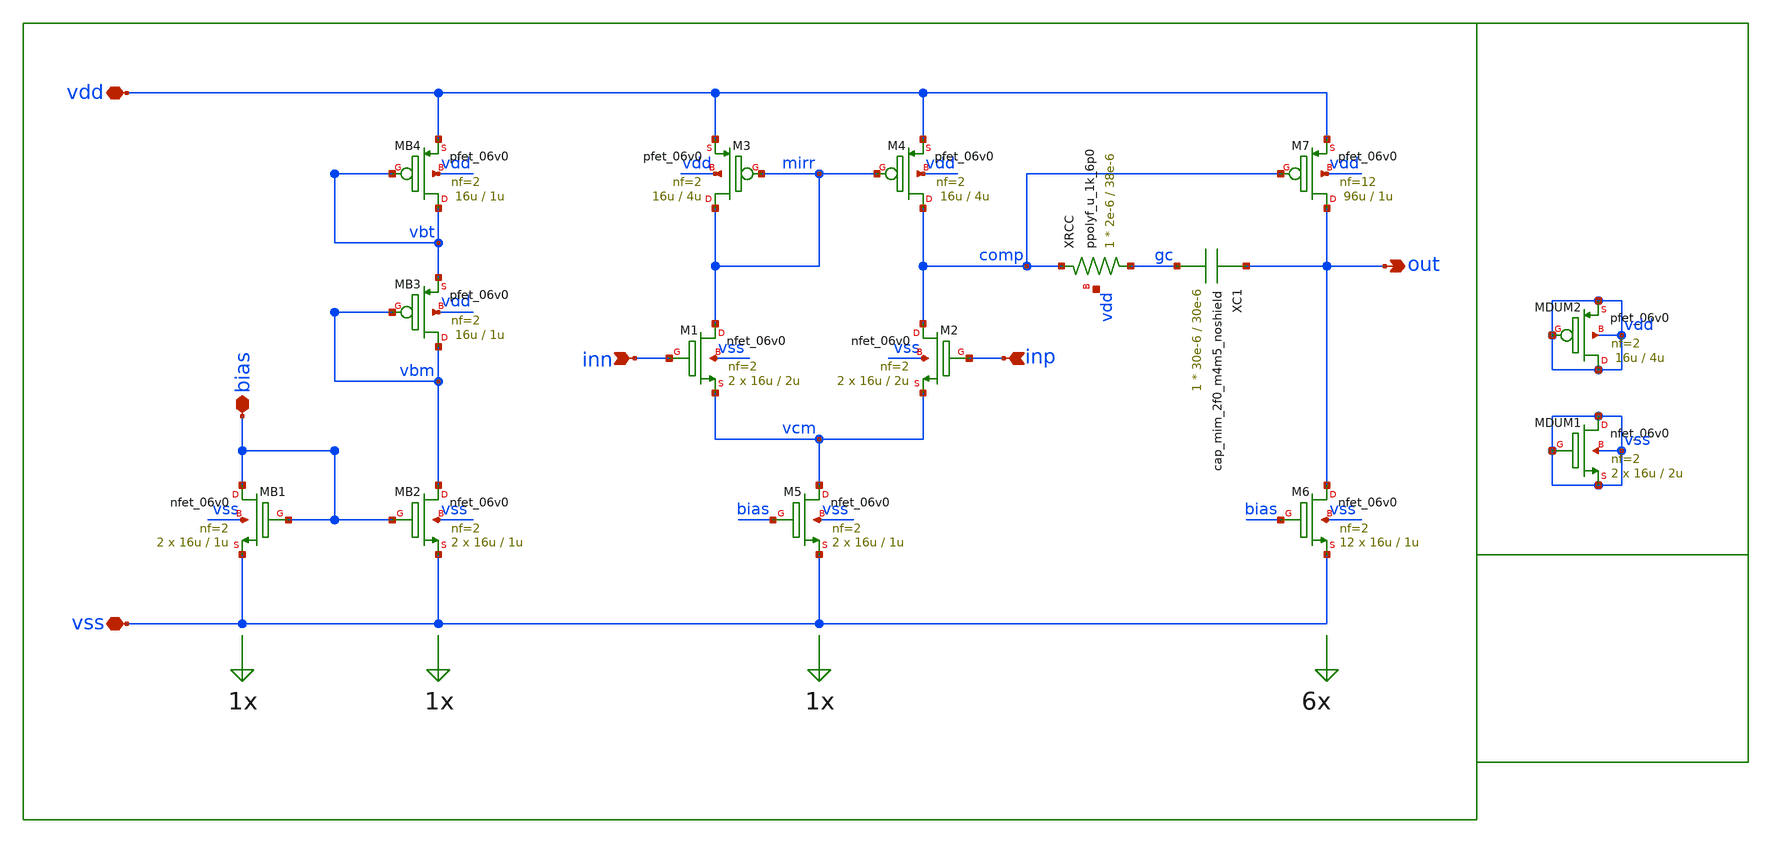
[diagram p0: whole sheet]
** sch_path: xschem/sch/testbuffer/tb_amplifier/tb_amplifier.sch
**.subckt tb_amplifier inn inp out bias vdd vss
*.ipin inn
*.ipin inp
*.opin out
*.iopin bias
*.iopin vdd
*.iopin vss
XM3 mirr mirr vdd vdd pfet_06v0 L=4u W=16u nf=2 ad='int((nf+1)/2) * W/nf * 0.18u' as='int((nf+2)/2) * W/nf * 0.18u'
+ pd='2*int((nf+1)/2) * (W/nf + 0.18u)' ps='2*int((nf+2)/2) * (W/nf + 0.18u)' nrd='0.18u / W' nrs='0.18u / W'
+ sa=0 sb=0 sd=0 m=2 par=2
XM4 comp mirr vdd vdd pfet_06v0 L=4u W=16u nf=2 ad='int((nf+1)/2) * W/nf * 0.18u' as='int((nf+2)/2) * W/nf * 0.18u'
+ pd='2*int((nf+1)/2) * (W/nf + 0.18u)' ps='2*int((nf+2)/2) * (W/nf + 0.18u)' nrd='0.18u / W' nrs='0.18u / W'
+ sa=0 sb=0 sd=0 m=2 par=2
XM2 comp inp vcm vss nfet_06v0 L=2u W=16u nf=2 ad='int((nf+1)/2) * W/nf * 0.18u' as='int((nf+2)/2) * W/nf * 0.18u'
+ pd='2*int((nf+1)/2) * (W/nf + 0.18u)' ps='2*int((nf+2)/2) * (W/nf + 0.18u)' nrd='0.18u / W' nrs='0.18u / W'
+ sa=0 sb=0 sd=0 m=2 par=2
XM1 mirr inn vcm vss nfet_06v0 L=2u W=16u nf=2 ad='int((nf+1)/2) * W/nf * 0.18u' as='int((nf+2)/2) * W/nf * 0.18u'
+ pd='2*int((nf+1)/2) * (W/nf + 0.18u)' ps='2*int((nf+2)/2) * (W/nf + 0.18u)' nrd='0.18u / W' nrs='0.18u / W'
+ sa=0 sb=0 sd=0 m=2 par=2
XM5 vcm bias vss vss nfet_06v0 L=1u W=16u nf=2 ad='int((nf+1)/2) * W/nf * 0.18u' as='int((nf+2)/2) * W/nf * 0.18u'
+ pd='2*int((nf+1)/2) * (W/nf + 0.18u)' ps='2*int((nf+2)/2) * (W/nf + 0.18u)' nrd='0.18u / W' nrs='0.18u / W'
+ sa=0 sb=0 sd=0 m=2 par=2
XM6 out bias vss vss nfet_06v0 L=1u W=16u nf=2 ad='int((nf+1)/2) * W/nf * 0.18u' as='int((nf+2)/2) * W/nf * 0.18u'
+ pd='2*int((nf+1)/2) * (W/nf + 0.18u)' ps='2*int((nf+2)/2) * (W/nf + 0.18u)' nrd='0.18u / W' nrs='0.18u / W'
+ sa=0 sb=0 sd=0 m=12 par=12
XM7 out comp vdd vdd pfet_06v0 L=1u W=96u nf=12 ad='int((nf+1)/2) * W/nf * 0.18u' as='int((nf+2)/2) * W/nf * 0.18u'
+ pd='2*int((nf+1)/2) * (W/nf + 0.18u)' ps='2*int((nf+2)/2) * (W/nf + 0.18u)' nrd='0.18u / W' nrs='0.18u / W'
+ sa=0 sb=0 sd=0 m=1 par=1
XMB1 bias bias vss vss nfet_06v0 L=1u W=16u nf=2 ad='int((nf+1)/2) * W/nf * 0.18u' as='int((nf+2)/2) * W/nf * 0.18u'
+ pd='2*int((nf+1)/2) * (W/nf + 0.18u)' ps='2*int((nf+2)/2) * (W/nf + 0.18u)' nrd='0.18u / W' nrs='0.18u / W'
+ sa=0 sb=0 sd=0 m=2 par=2
XMB2 vbm bias vss vss nfet_06v0 L=1u W=16u nf=2 ad='int((nf+1)/2) * W/nf * 0.18u' as='int((nf+2)/2) * W/nf * 0.18u'
+ pd='2*int((nf+1)/2) * (W/nf + 0.18u)' ps='2*int((nf+2)/2) * (W/nf + 0.18u)' nrd='0.18u / W' nrs='0.18u / W'
+ sa=0 sb=0 sd=0 m=2 par=2
XMB3 vbm vbm vbt vdd pfet_06v0 L=1u W=16u nf=2 ad='int((nf+1)/2) * W/nf * 0.18u' as='int((nf+2)/2) * W/nf * 0.18u'
+ pd='2*int((nf+1)/2) * (W/nf + 0.18u)' ps='2*int((nf+2)/2) * (W/nf + 0.18u)' nrd='0.18u / W' nrs='0.18u / W'
+ sa=0 sb=0 sd=0 m=1 par=1
XMB4 vbt vbt vdd vdd pfet_06v0 L=1u W=16u nf=2 ad='int((nf+1)/2) * W/nf * 0.18u' as='int((nf+2)/2) * W/nf * 0.18u'
+ pd='2*int((nf+1)/2) * (W/nf + 0.18u)' ps='2*int((nf+2)/2) * (W/nf + 0.18u)' nrd='0.18u / W' nrs='0.18u / W'
+ sa=0 sb=0 sd=0 m=1 par=1
XRCC gc comp vdd ppolyf_u_1k_6p0 r_width=2e-6 r_length=38e-6 s=1 m=1
XMDUM1 vss vss vss vss nfet_06v0 L=2u W=16u nf=2 ad='int((nf+1)/2) * W/nf * 0.18u' as='int((nf+2)/2) * W/nf * 0.18u'
+ pd='2*int((nf+1)/2) * (W/nf + 0.18u)' ps='2*int((nf+2)/2) * (W/nf + 0.18u)' nrd='0.18u / W' nrs='0.18u / W'
+ sa=0 sb=0 sd=0 m=2 par=2
XMDUM2 vdd vdd vdd vdd pfet_06v0 L=4u W=16u nf=2 ad='int((nf+1)/2) * W/nf * 0.18u' as='int((nf+2)/2) * W/nf * 0.18u'
+ pd='2*int((nf+1)/2) * (W/nf + 0.18u)' ps='2*int((nf+2)/2) * (W/nf + 0.18u)' nrd='0.18u / W' nrs='0.18u / W'
+ sa=0 sb=0 sd=0 m=4 par=4
XC1 out gc cap_mim_2f0_m4m5_noshield c_width=30e-6 c_length=30e-6 m=1
**.ends
.end
